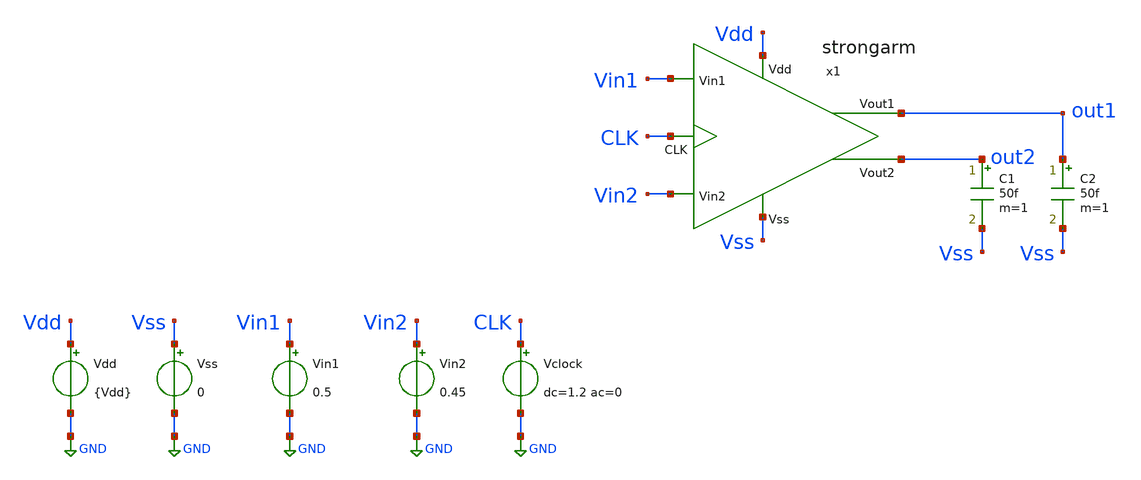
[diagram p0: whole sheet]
** sch_path: xschem/TB/TB_Op_SA.sch
**.subckt TB_Op_SA
Vdd Vdd GND {Vdd}
x1 out2 out1 Vdd Vss Vin2 Vin1 CLK strongarm
Vss Vss GND 0
C1 out2 Vss 50f m=1
C2 out1 Vss 50f m=1
Vin1 Vin1 GND 0.5
Vin2 Vin2 GND 0.45
Vclock CLK GND dc=1.2 ac=0
**** begin user architecture code


.param Vdd = 1.2
.param ACM = 10m
.param FCM = 10MEG
.param VCM = 0.6





.lib cornerMOSlv.lib mos_tt




** TRANSISTORES NMOS

.param W12 = 1.0u
.param L12 = 0.13u
.param M12 = 1

.param W34 = 1.0u
.param L34 = 0.13u
.param M34 = 1

.param W56 = 1.0u
.param L56 = 0.13u
.param M56 = 1

.param W7  = 1.0u
.param L7  = 0.13u
.param M7  = 1

.param W89 = 1.0u
.param L89 = 0.13u
.param M89 = 1

.param Wab = 1.0u
.param Lab = 0.13u
.param Mab = 1




.control
save all  @n.x1.xm1.nsg13_lv_nmos[gm]  @n.x1.xm2.nsg13_lv_nmos[gm]  @n.x1.xm1.nsg13_lv_nmos[ids]
+  @n.x1.xm2.nsg13_lv_nmos[ids]
op
let CP   = @n.x1.xm1.nsg13_lv_nmos[cdd] + @n.x1.xm1.nsg13_lv_nmos[cdb] +
+ @n.x1.xm1.nsg13_lv_nmos[cgdol]
let CQ   = @n.x1.xm2.nsg13_lv_nmos[cdd] + @n.x1.xm2.nsg13_lv_nmos[cdb] +
+ @n.x1.xm2.nsg13_lv_nmos[cgdol]
let gm1  = @n.x1.xm1.nsg13_lv_nmos[gm]
let gm2  = @n.x1.xm2.nsg13_lv_nmos[gm]
let rds1 = 1/@n.x1.xm1.nsg13_lv_nmos[gds]
let rds2 = 1/@n.x1.xm2.nsg13_lv_nmos[gds]
let Av1  = gm1*rds1
let Av2  = gm2*rds2
print CP CQ
print
print Av1 Av2
print v(vout1)
.endc


**** end user architecture code
**.ends

* expanding   symbol:  ../sch/strongarm.sym # of pins=7
** sym_path: xschem/sch/strongarm.sym
** sch_path: xschem/sch/strongarm.sch
.subckt strongarm Vout2 Vout1 Vdd Vss Vin2 Vin1 CLK
*.opin Vout2
*.opin Vout1
*.ipin Vin1
*.ipin Vin2
*.ipin CLK
*.ipin Vss
*.ipin Vdd
XM1 net1 Vin1 P Vss sg13_lv_nmos w={W12} l={L12} ng=1 m={M12} mm_ok=1
XM2 net1 Vin2 Q Vss sg13_lv_nmos w={W12} l={L12} ng=1 m={M12} mm_ok=1
XM3 P Vout2 Vout1 Vss sg13_lv_nmos w={W34} l={L34} ng=1 m={M34} mm_ok=1
XM4 Q Vout1 Vout2 Vss sg13_lv_nmos w={W34} l={L34} ng=1 m={M34} mm_ok=1
XM6 Vout2 Vout1 Vdd Vdd sg13_lv_pmos w=1.0u l=0.45u ng=1 m=1 mm_ok=1
XM5 Vout1 Vout2 Vdd Vdd sg13_lv_pmos w={W56} l={L56} ng=1 m={M56} mm_ok=1
XM7 Vss CLK net1 Vss sg13_lv_nmos w={W7} l={L7} ng=1 m={M7} mm_ok=1
XM8 P CLK Vdd Vdd sg13_lv_pmos w={W89} l={L89} ng=1 m={M89} mm_ok=1
XM9 Q CLK Vdd Vdd sg13_lv_pmos w={W89} l={L89} ng=1 m={M89} mm_ok=1
XM11 Vout2 CLK Vdd Vdd sg13_lv_pmos w={Wab} l={Lab} ng=1 m={Wab} mm_ok=1
XM10 Vout1 CLK Vdd Vdd sg13_lv_pmos w={Wab} l={Lab} ng=1 m={Wab} mm_ok=1
.ends

.GLOBAL GND
.end
